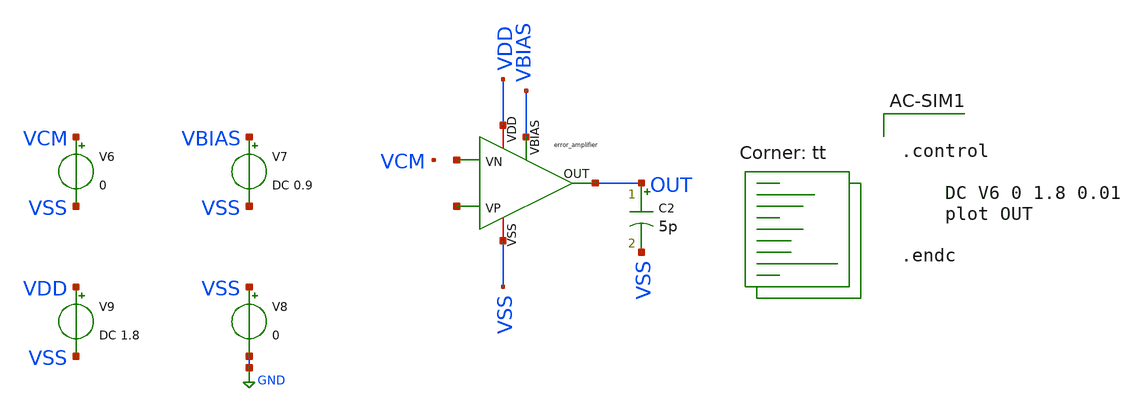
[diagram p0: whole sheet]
** sch_path: LDO_UVLO_Design/testbench/tb_error-amplifier/tran-response.sch
**.subckt tran-response
V6 VCM VSS 0
V7 VBIAS VSS DC 0.9
V8 VSS GND 0
V9 VDD VSS DC 1.8
C2 OUT VSS 5p m=1
x1 VDD VBIAS net1 net2 OUT VSS error_amplifier
**** begin user architecture code
.lib $::SKYWATER_MODELS/sky130.lib.spice tt


.control

	DC V6 0 1.8 0.01
	plot OUT

.endc


**** end user architecture code
**.ends

* expanding   symbol:  ldo-sky130A-its/LDO_UVLO_Design/schematics/error_amplifier.sym # of pins=6
** sym_path: LDO_UVLO_Design/schematics/error_amplifier.sym
** sch_path: LDO_UVLO_Design/schematics/error_amplifier.sch
.subckt error_amplifier VDD VBIAS VP VN OUT VSS
*.iopin VDD
*.iopin VSS
*.ipin VBIAS
*.ipin VP
*.ipin VN
*.opin OUT
XM1 net2 net2 VSS VSS sky130_fd_pr__nfet_01v8 L=1.5 W=12 nf=1 ad='int((nf+1)/2) * W/nf * 0.29' as='int((nf+2)/2) * W/nf * 0.29'
+ pd='2*int((nf+1)/2) * (W/nf + 0.29)' ps='2*int((nf+2)/2) * (W/nf + 0.29)' nrd='0.29 / W' nrs='0.29 / W'
+ sa=0 sb=0 sd=0 mult=1 m=1
XM2 net1 net1 VSS VSS sky130_fd_pr__nfet_01v8 L=1.5 W=12 nf=1 ad='int((nf+1)/2) * W/nf * 0.29' as='int((nf+2)/2) * W/nf * 0.29'
+ pd='2*int((nf+1)/2) * (W/nf + 0.29)' ps='2*int((nf+2)/2) * (W/nf + 0.29)' nrd='0.29 / W' nrs='0.29 / W'
+ sa=0 sb=0 sd=0 mult=1 m=1
XM3 net2 VP net4 VDD sky130_fd_pr__pfet_01v8 L=1.5 W=12 nf=1 ad='int((nf+1)/2) * W/nf * 0.29' as='int((nf+2)/2) * W/nf * 0.29'
+ pd='2*int((nf+1)/2) * (W/nf + 0.29)' ps='2*int((nf+2)/2) * (W/nf + 0.29)' nrd='0.29 / W' nrs='0.29 / W'
+ sa=0 sb=0 sd=0 mult=1 m=1
XM4 net1 VN net4 VDD sky130_fd_pr__pfet_01v8 L=1.5 W=12 nf=1 ad='int((nf+1)/2) * W/nf * 0.29' as='int((nf+2)/2) * W/nf * 0.29'
+ pd='2*int((nf+1)/2) * (W/nf + 0.29)' ps='2*int((nf+2)/2) * (W/nf + 0.29)' nrd='0.29 / W' nrs='0.29 / W'
+ sa=0 sb=0 sd=0 mult=1 m=1
XM7 net3 net1 VSS VSS sky130_fd_pr__nfet_01v8 L=1.5 W=12 nf=1 ad='int((nf+1)/2) * W/nf * 0.29' as='int((nf+2)/2) * W/nf * 0.29'
+ pd='2*int((nf+1)/2) * (W/nf + 0.29)' ps='2*int((nf+2)/2) * (W/nf + 0.29)' nrd='0.29 / W' nrs='0.29 / W'
+ sa=0 sb=0 sd=0 mult=1 m=1
XM8 OUT net2 VSS VSS sky130_fd_pr__nfet_01v8 L=1.5 W=12 nf=1 ad='int((nf+1)/2) * W/nf * 0.29' as='int((nf+2)/2) * W/nf * 0.29'
+ pd='2*int((nf+1)/2) * (W/nf + 0.29)' ps='2*int((nf+2)/2) * (W/nf + 0.29)' nrd='0.29 / W' nrs='0.29 / W'
+ sa=0 sb=0 sd=0 mult=1 m=1
XM9 net3 net3 VDD VDD sky130_fd_pr__pfet_01v8 L=1.5 W=12 nf=1 ad='int((nf+1)/2) * W/nf * 0.29' as='int((nf+2)/2) * W/nf * 0.29'
+ pd='2*int((nf+1)/2) * (W/nf + 0.29)' ps='2*int((nf+2)/2) * (W/nf + 0.29)' nrd='0.29 / W' nrs='0.29 / W'
+ sa=0 sb=0 sd=0 mult=1 m=1
XM10 OUT net3 VDD VDD sky130_fd_pr__pfet_01v8 L=1.5 W=12 nf=1 ad='int((nf+1)/2) * W/nf * 0.29' as='int((nf+2)/2) * W/nf * 0.29'
+ pd='2*int((nf+1)/2) * (W/nf + 0.29)' ps='2*int((nf+2)/2) * (W/nf + 0.29)' nrd='0.29 / W' nrs='0.29 / W'
+ sa=0 sb=0 sd=0 mult=1 m=1
XM11 net4 VBIAS VDD VDD sky130_fd_pr__pfet_01v8 L=1.5 W=12 nf=1 ad='int((nf+1)/2) * W/nf * 0.29' as='int((nf+2)/2) * W/nf * 0.29'
+ pd='2*int((nf+1)/2) * (W/nf + 0.29)' ps='2*int((nf+2)/2) * (W/nf + 0.29)' nrd='0.29 / W' nrs='0.29 / W'
+ sa=0 sb=0 sd=0 mult=1 m=1
.ends

.GLOBAL GND
.end
